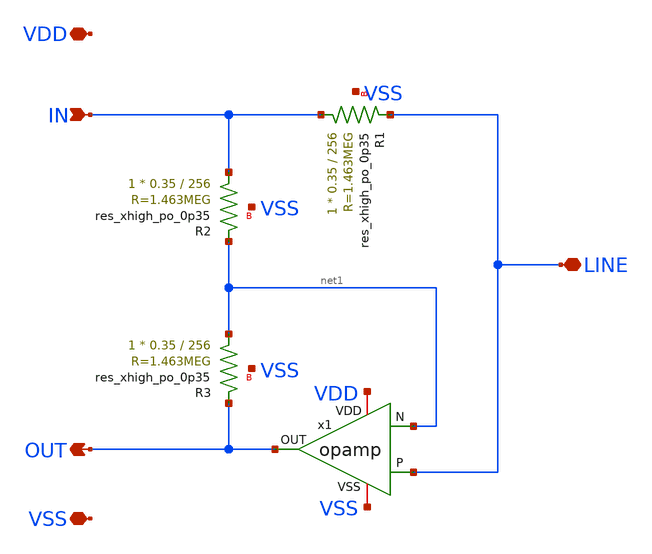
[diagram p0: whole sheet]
** sch_path: xschem/hybrid.sch
**.subckt hybrid VDD VSS IN OUT LINE
*.iopin VDD
*.iopin VSS
*.ipin IN
*.opin OUT
*.iopin LINE
x1 VDD OUT LINE net1 VSS opamp
XR1 IN LINE VSS sky130_fd_pr__res_xhigh_po_0p35 L=256 mult=1 m=1
XR2 IN net1 VSS sky130_fd_pr__res_xhigh_po_0p35 L=256 mult=1 m=1
XR3 net1 OUT VSS sky130_fd_pr__res_xhigh_po_0p35 L=256 mult=1 m=1
**.ends

* expanding   symbol:  opamp.sym # of pins=5
** sym_path: xschem/opamp.sym
** sch_path: xschem/opamp.sch
.subckt opamp VDD OUT P N VSS
*.iopin VDD
*.iopin VSS
*.ipin P
*.ipin N
*.opin OUT
XR1 net2 VDD VSS sky130_fd_pr__res_xhigh_po_0p35 L=25 mult=1 m=1
XM1 net2 net2 VSS VSS sky130_fd_pr__nfet_g5v0d10v5 L=1 W=2 nf=1 ad='int((1 + 1)/2) * 2 / 1 * 0.29' as='int((1 + 2)/2) * 2 / 1 * 0.29'
+ pd='2*int((1 + 1)/2) * (2 / 1 + 0.29)' ps='2*int((1 + 2)/2) * (2 / 1 + 0.29)' nrd='0.29 / 2 ' nrs='0.29 / 2 '
+ sa=0 sb=0 sd=0 mult=2 m=2
XM7 net1 net1 VDD VDD sky130_fd_pr__pfet_g5v0d10v5 L=1 W=4 nf=1 ad='int((1 + 1)/2) * 4 / 1 * 0.29' as='int((1 + 2)/2) * 4 / 1 * 0.29'
+ pd='2*int((1 + 1)/2) * (4 / 1 + 0.29)' ps='2*int((1 + 2)/2) * (4 / 1 + 0.29)' nrd='0.29 / 4 ' nrs='0.29 / 4 '
+ sa=0 sb=0 sd=0 mult=2 m=2
XM8 OUT net1 VDD VDD sky130_fd_pr__pfet_g5v0d10v5 L=1 W=4 nf=1 ad='int((1 + 1)/2) * 4 / 1 * 0.29' as='int((1 + 2)/2) * 4 / 1 * 0.29'
+ pd='2*int((1 + 1)/2) * (4 / 1 + 0.29)' ps='2*int((1 + 2)/2) * (4 / 1 + 0.29)' nrd='0.29 / 4 ' nrs='0.29 / 4 '
+ sa=0 sb=0 sd=0 mult=2 m=2
XM4 net6 net2 VSS VSS sky130_fd_pr__nfet_g5v0d10v5 L=1 W=2 nf=1 ad='int((1 + 1)/2) * 2 / 1 * 0.29' as='int((1 + 2)/2) * 2 / 1 * 0.29'
+ pd='2*int((1 + 1)/2) * (2 / 1 + 0.29)' ps='2*int((1 + 2)/2) * (2 / 1 + 0.29)' nrd='0.29 / 2 ' nrs='0.29 / 2 '
+ sa=0 sb=0 sd=0 mult=2 m=2
XM5 net1 P net6 VSS sky130_fd_pr__nfet_g5v0d10v5 L=1 W=2 nf=1 ad='int((1 + 1)/2) * 2 / 1 * 0.29' as='int((1 + 2)/2) * 2 / 1 * 0.29'
+ pd='2*int((1 + 1)/2) * (2 / 1 + 0.29)' ps='2*int((1 + 2)/2) * (2 / 1 + 0.29)' nrd='0.29 / 2 ' nrs='0.29 / 2 '
+ sa=0 sb=0 sd=0 mult=2 m=2
XM6 OUT N net6 VSS sky130_fd_pr__nfet_g5v0d10v5 L=1 W=2 nf=1 ad='int((1 + 1)/2) * 2 / 1 * 0.29' as='int((1 + 2)/2) * 2 / 1 * 0.29'
+ pd='2*int((1 + 1)/2) * (2 / 1 + 0.29)' ps='2*int((1 + 2)/2) * (2 / 1 + 0.29)' nrd='0.29 / 2 ' nrs='0.29 / 2 '
+ sa=0 sb=0 sd=0 mult=2 m=2
XM2 net5 net2 VSS VSS sky130_fd_pr__nfet_g5v0d10v5 L=1 W=2 nf=1 ad='int((1 + 1)/2) * 2 / 1 * 0.29' as='int((1 + 2)/2) * 2 / 1 * 0.29'
+ pd='2*int((1 + 1)/2) * (2 / 1 + 0.29)' ps='2*int((1 + 2)/2) * (2 / 1 + 0.29)' nrd='0.29 / 2 ' nrs='0.29 / 2 '
+ sa=0 sb=0 sd=0 mult=2 m=2
XM9 net4 net5 VDD VDD sky130_fd_pr__pfet_g5v0d10v5 L=1 W=4 nf=1 ad='int((1 + 1)/2) * 4 / 1 * 0.29' as='int((1 + 2)/2) * 4 / 1 * 0.29'
+ pd='2*int((1 + 1)/2) * (4 / 1 + 0.29)' ps='2*int((1 + 2)/2) * (4 / 1 + 0.29)' nrd='0.29 / 4 ' nrs='0.29 / 4 '
+ sa=0 sb=0 sd=0 mult=2 m=2
XM3 VDD net5 net5 VDD sky130_fd_pr__pfet_g5v0d10v5 L=1 W=4 nf=1 ad='int((1 + 1)/2) * 4 / 1 * 0.29' as='int((1 + 2)/2) * 4 / 1 * 0.29'
+ pd='2*int((1 + 1)/2) * (4 / 1 + 0.29)' ps='2*int((1 + 2)/2) * (4 / 1 + 0.29)' nrd='0.29 / 4 ' nrs='0.29 / 4 '
+ sa=0 sb=0 sd=0 mult=2 m=2
XM10 net3 P net4 VDD sky130_fd_pr__pfet_g5v0d10v5 L=1 W=4 nf=1 ad='int((1 + 1)/2) * 4 / 1 * 0.29' as='int((1 + 2)/2) * 4 / 1 * 0.29'
+ pd='2*int((1 + 1)/2) * (4 / 1 + 0.29)' ps='2*int((1 + 2)/2) * (4 / 1 + 0.29)' nrd='0.29 / 4 ' nrs='0.29 / 4 '
+ sa=0 sb=0 sd=0 mult=2 m=2
XM11 OUT N net4 VDD sky130_fd_pr__pfet_g5v0d10v5 L=1 W=4 nf=1 ad='int((1 + 1)/2) * 4 / 1 * 0.29' as='int((1 + 2)/2) * 4 / 1 * 0.29'
+ pd='2*int((1 + 1)/2) * (4 / 1 + 0.29)' ps='2*int((1 + 2)/2) * (4 / 1 + 0.29)' nrd='0.29 / 4 ' nrs='0.29 / 4 '
+ sa=0 sb=0 sd=0 mult=2 m=2
XM12 net3 net3 VSS VSS sky130_fd_pr__nfet_g5v0d10v5 L=1 W=2 nf=1 ad='int((1 + 1)/2) * 2 / 1 * 0.29' as='int((1 + 2)/2) * 2 / 1 * 0.29'
+ pd='2*int((1 + 1)/2) * (2 / 1 + 0.29)' ps='2*int((1 + 2)/2) * (2 / 1 + 0.29)' nrd='0.29 / 2 ' nrs='0.29 / 2 '
+ sa=0 sb=0 sd=0 mult=2 m=2
XM13 OUT net3 VSS VSS sky130_fd_pr__nfet_g5v0d10v5 L=1 W=2 nf=1 ad='int((1 + 1)/2) * 2 / 1 * 0.29' as='int((1 + 2)/2) * 2 / 1 * 0.29'
+ pd='2*int((1 + 1)/2) * (2 / 1 + 0.29)' ps='2*int((1 + 2)/2) * (2 / 1 + 0.29)' nrd='0.29 / 2 ' nrs='0.29 / 2 '
+ sa=0 sb=0 sd=0 mult=2 m=2
.ends

.end
